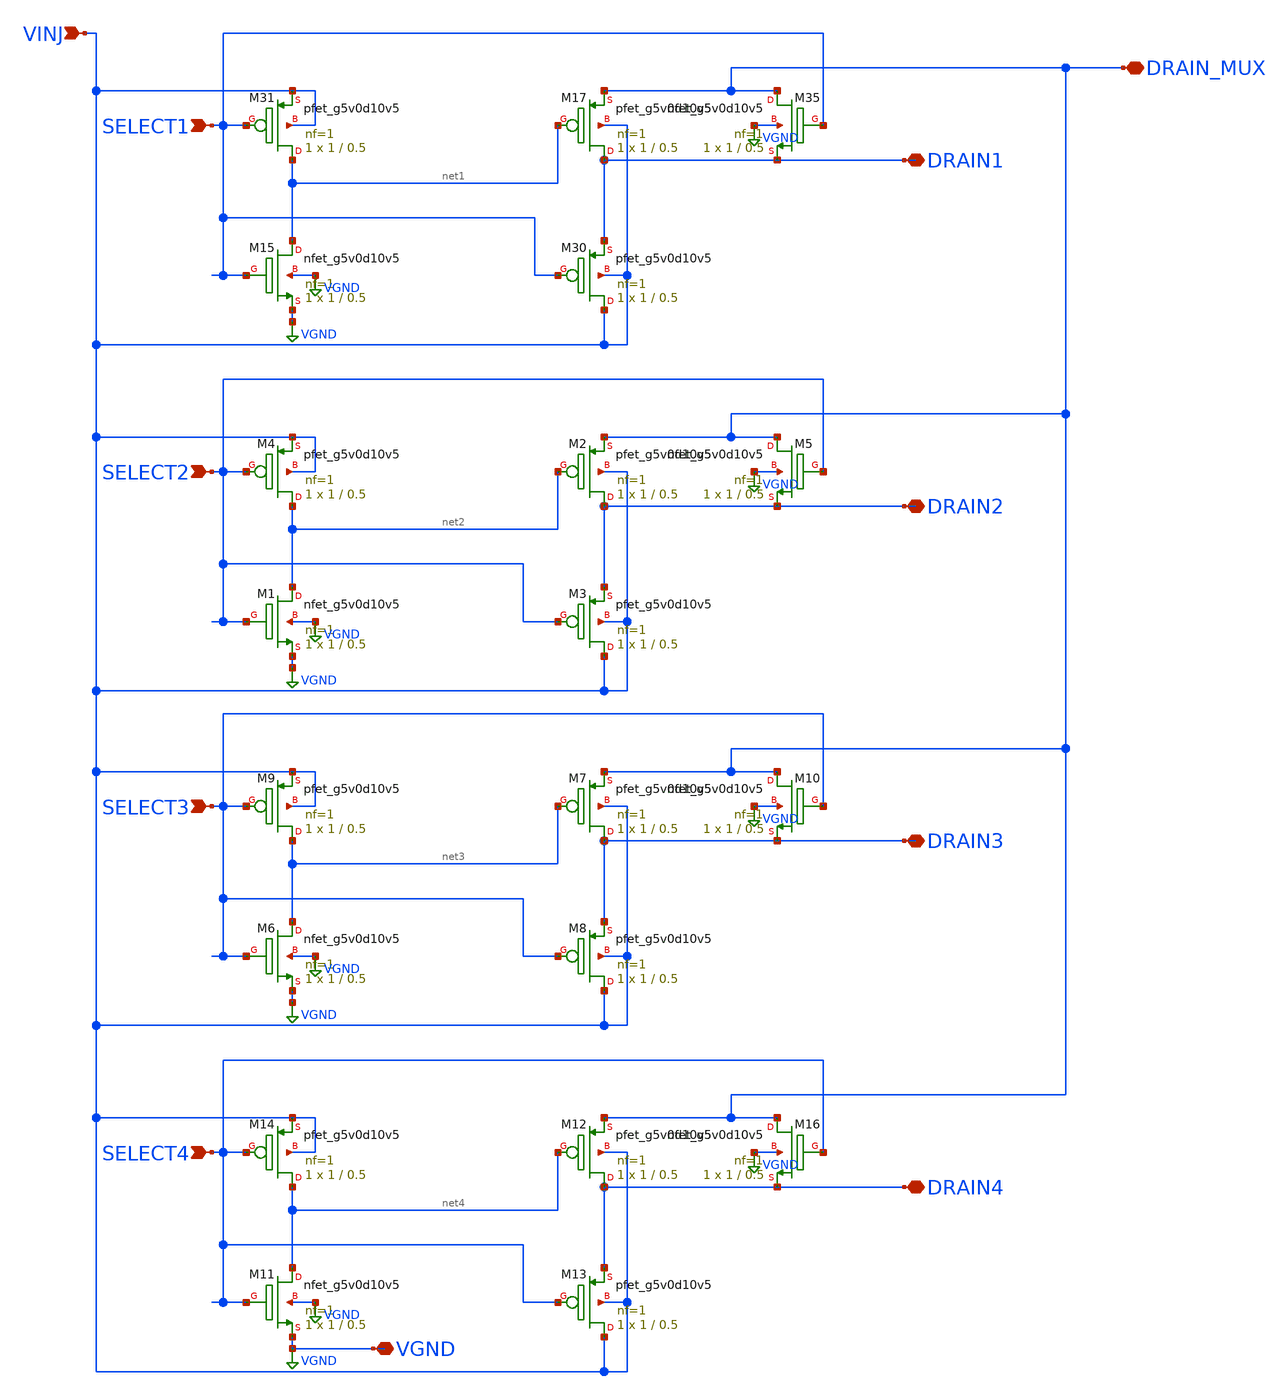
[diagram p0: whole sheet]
** sch_path: sky130_cells/Practice/DrainSelect/sky130_hilas_drainSelect01d3ActiveHigh.sch
**.subckt sky130_hilas_drainSelect01d3ActiveHigh SELECT1 DRAIN_MUX DRAIN1 VINJ SELECT2 DRAIN2
*+ SELECT3 DRAIN3 SELECT4 DRAIN4 VGND
*.ipin SELECT1
*.iopin DRAIN_MUX
*.iopin DRAIN1
*.ipin VINJ
*.ipin SELECT2
*.iopin DRAIN2
*.ipin SELECT3
*.iopin DRAIN3
*.ipin SELECT4
*.iopin DRAIN4
*.iopin VGND
XM15 net1 SELECT1 VGND VGND sky130_fd_pr__nfet_g5v0d10v5 L=0.5 W=1 nf=1 ad='int((nf+1)/2) * W/nf * 0.29'
+ as='int((nf+2)/2) * W/nf * 0.29' pd='2*int((nf+1)/2) * (W/nf + 0.29)' ps='2*int((nf+2)/2) * (W/nf + 0.29)'
+ nrd='0.29 / W' nrs='0.29 / W' sa=0 sb=0 sd=0 mult=1 m=1
XM17 DRAIN1 net1 DRAIN_MUX VINJ sky130_fd_pr__pfet_g5v0d10v5 L=0.5 W=1 nf=1 ad='int((nf+1)/2) * W/nf * 0.29'
+ as='int((nf+2)/2) * W/nf * 0.29' pd='2*int((nf+1)/2) * (W/nf + 0.29)' ps='2*int((nf+2)/2) * (W/nf + 0.29)'
+ nrd='0.29 / W' nrs='0.29 / W' sa=0 sb=0 sd=0 mult=1 m=1
XM30 VINJ SELECT1 DRAIN1 VINJ sky130_fd_pr__pfet_g5v0d10v5 L=0.5 W=1 nf=1 ad='int((nf+1)/2) * W/nf * 0.29'
+ as='int((nf+2)/2) * W/nf * 0.29' pd='2*int((nf+1)/2) * (W/nf + 0.29)' ps='2*int((nf+2)/2) * (W/nf + 0.29)'
+ nrd='0.29 / W' nrs='0.29 / W' sa=0 sb=0 sd=0 mult=1 m=1
XM31 net1 SELECT1 VINJ VINJ sky130_fd_pr__pfet_g5v0d10v5 L=0.5 W=1 nf=1 ad='int((nf+1)/2) * W/nf * 0.29'
+ as='int((nf+2)/2) * W/nf * 0.29' pd='2*int((nf+1)/2) * (W/nf + 0.29)' ps='2*int((nf+2)/2) * (W/nf + 0.29)'
+ nrd='0.29 / W' nrs='0.29 / W' sa=0 sb=0 sd=0 mult=1 m=1
XM35 DRAIN_MUX SELECT1 DRAIN1 VGND sky130_fd_pr__nfet_g5v0d10v5 L=0.5 W=1 nf=1 ad='int((nf+1)/2) * W/nf * 0.29'
+ as='int((nf+2)/2) * W/nf * 0.29' pd='2*int((nf+1)/2) * (W/nf + 0.29)' ps='2*int((nf+2)/2) * (W/nf + 0.29)'
+ nrd='0.29 / W' nrs='0.29 / W' sa=0 sb=0 sd=0 mult=1 m=1
XM1 net2 SELECT2 VGND VGND sky130_fd_pr__nfet_g5v0d10v5 L=0.5 W=1 nf=1 ad='int((nf+1)/2) * W/nf * 0.29'
+ as='int((nf+2)/2) * W/nf * 0.29' pd='2*int((nf+1)/2) * (W/nf + 0.29)' ps='2*int((nf+2)/2) * (W/nf + 0.29)'
+ nrd='0.29 / W' nrs='0.29 / W' sa=0 sb=0 sd=0 mult=1 m=1
XM2 DRAIN2 net2 DRAIN_MUX VINJ sky130_fd_pr__pfet_g5v0d10v5 L=0.5 W=1 nf=1 ad='int((nf+1)/2) * W/nf * 0.29'
+ as='int((nf+2)/2) * W/nf * 0.29' pd='2*int((nf+1)/2) * (W/nf + 0.29)' ps='2*int((nf+2)/2) * (W/nf + 0.29)'
+ nrd='0.29 / W' nrs='0.29 / W' sa=0 sb=0 sd=0 mult=1 m=1
XM3 VINJ SELECT2 DRAIN2 VINJ sky130_fd_pr__pfet_g5v0d10v5 L=0.5 W=1 nf=1 ad='int((nf+1)/2) * W/nf * 0.29'
+ as='int((nf+2)/2) * W/nf * 0.29' pd='2*int((nf+1)/2) * (W/nf + 0.29)' ps='2*int((nf+2)/2) * (W/nf + 0.29)'
+ nrd='0.29 / W' nrs='0.29 / W' sa=0 sb=0 sd=0 mult=1 m=1
XM4 net2 SELECT2 VINJ VINJ sky130_fd_pr__pfet_g5v0d10v5 L=0.5 W=1 nf=1 ad='int((nf+1)/2) * W/nf * 0.29'
+ as='int((nf+2)/2) * W/nf * 0.29' pd='2*int((nf+1)/2) * (W/nf + 0.29)' ps='2*int((nf+2)/2) * (W/nf + 0.29)'
+ nrd='0.29 / W' nrs='0.29 / W' sa=0 sb=0 sd=0 mult=1 m=1
XM5 DRAIN_MUX SELECT2 DRAIN2 VGND sky130_fd_pr__nfet_g5v0d10v5 L=0.5 W=1 nf=1 ad='int((nf+1)/2) * W/nf * 0.29'
+ as='int((nf+2)/2) * W/nf * 0.29' pd='2*int((nf+1)/2) * (W/nf + 0.29)' ps='2*int((nf+2)/2) * (W/nf + 0.29)'
+ nrd='0.29 / W' nrs='0.29 / W' sa=0 sb=0 sd=0 mult=1 m=1
XM6 net3 SELECT3 VGND VGND sky130_fd_pr__nfet_g5v0d10v5 L=0.5 W=1 nf=1 ad='int((nf+1)/2) * W/nf * 0.29'
+ as='int((nf+2)/2) * W/nf * 0.29' pd='2*int((nf+1)/2) * (W/nf + 0.29)' ps='2*int((nf+2)/2) * (W/nf + 0.29)'
+ nrd='0.29 / W' nrs='0.29 / W' sa=0 sb=0 sd=0 mult=1 m=1
XM7 DRAIN3 net3 DRAIN_MUX VINJ sky130_fd_pr__pfet_g5v0d10v5 L=0.5 W=1 nf=1 ad='int((nf+1)/2) * W/nf * 0.29'
+ as='int((nf+2)/2) * W/nf * 0.29' pd='2*int((nf+1)/2) * (W/nf + 0.29)' ps='2*int((nf+2)/2) * (W/nf + 0.29)'
+ nrd='0.29 / W' nrs='0.29 / W' sa=0 sb=0 sd=0 mult=1 m=1
XM8 VINJ SELECT3 DRAIN3 VINJ sky130_fd_pr__pfet_g5v0d10v5 L=0.5 W=1 nf=1 ad='int((nf+1)/2) * W/nf * 0.29'
+ as='int((nf+2)/2) * W/nf * 0.29' pd='2*int((nf+1)/2) * (W/nf + 0.29)' ps='2*int((nf+2)/2) * (W/nf + 0.29)'
+ nrd='0.29 / W' nrs='0.29 / W' sa=0 sb=0 sd=0 mult=1 m=1
XM9 net3 SELECT3 VINJ VINJ sky130_fd_pr__pfet_g5v0d10v5 L=0.5 W=1 nf=1 ad='int((nf+1)/2) * W/nf * 0.29'
+ as='int((nf+2)/2) * W/nf * 0.29' pd='2*int((nf+1)/2) * (W/nf + 0.29)' ps='2*int((nf+2)/2) * (W/nf + 0.29)'
+ nrd='0.29 / W' nrs='0.29 / W' sa=0 sb=0 sd=0 mult=1 m=1
XM10 DRAIN_MUX SELECT3 DRAIN3 VGND sky130_fd_pr__nfet_g5v0d10v5 L=0.5 W=1 nf=1 ad='int((nf+1)/2) * W/nf * 0.29'
+ as='int((nf+2)/2) * W/nf * 0.29' pd='2*int((nf+1)/2) * (W/nf + 0.29)' ps='2*int((nf+2)/2) * (W/nf + 0.29)'
+ nrd='0.29 / W' nrs='0.29 / W' sa=0 sb=0 sd=0 mult=1 m=1
XM11 net4 SELECT4 VGND VGND sky130_fd_pr__nfet_g5v0d10v5 L=0.5 W=1 nf=1 ad='int((nf+1)/2) * W/nf * 0.29'
+ as='int((nf+2)/2) * W/nf * 0.29' pd='2*int((nf+1)/2) * (W/nf + 0.29)' ps='2*int((nf+2)/2) * (W/nf + 0.29)'
+ nrd='0.29 / W' nrs='0.29 / W' sa=0 sb=0 sd=0 mult=1 m=1
XM12 DRAIN4 net4 DRAIN_MUX VINJ sky130_fd_pr__pfet_g5v0d10v5 L=0.5 W=1 nf=1 ad='int((nf+1)/2) * W/nf * 0.29'
+ as='int((nf+2)/2) * W/nf * 0.29' pd='2*int((nf+1)/2) * (W/nf + 0.29)' ps='2*int((nf+2)/2) * (W/nf + 0.29)'
+ nrd='0.29 / W' nrs='0.29 / W' sa=0 sb=0 sd=0 mult=1 m=1
XM13 VINJ SELECT4 DRAIN4 VINJ sky130_fd_pr__pfet_g5v0d10v5 L=0.5 W=1 nf=1 ad='int((nf+1)/2) * W/nf * 0.29'
+ as='int((nf+2)/2) * W/nf * 0.29' pd='2*int((nf+1)/2) * (W/nf + 0.29)' ps='2*int((nf+2)/2) * (W/nf + 0.29)'
+ nrd='0.29 / W' nrs='0.29 / W' sa=0 sb=0 sd=0 mult=1 m=1
XM14 net4 SELECT4 VINJ VINJ sky130_fd_pr__pfet_g5v0d10v5 L=0.5 W=1 nf=1 ad='int((nf+1)/2) * W/nf * 0.29'
+ as='int((nf+2)/2) * W/nf * 0.29' pd='2*int((nf+1)/2) * (W/nf + 0.29)' ps='2*int((nf+2)/2) * (W/nf + 0.29)'
+ nrd='0.29 / W' nrs='0.29 / W' sa=0 sb=0 sd=0 mult=1 m=1
XM16 DRAIN_MUX SELECT4 DRAIN4 VGND sky130_fd_pr__nfet_g5v0d10v5 L=0.5 W=1 nf=1 ad='int((nf+1)/2) * W/nf * 0.29'
+ as='int((nf+2)/2) * W/nf * 0.29' pd='2*int((nf+1)/2) * (W/nf + 0.29)' ps='2*int((nf+2)/2) * (W/nf + 0.29)'
+ nrd='0.29 / W' nrs='0.29 / W' sa=0 sb=0 sd=0 mult=1 m=1
**.ends
.GLOBAL VGND
.end
